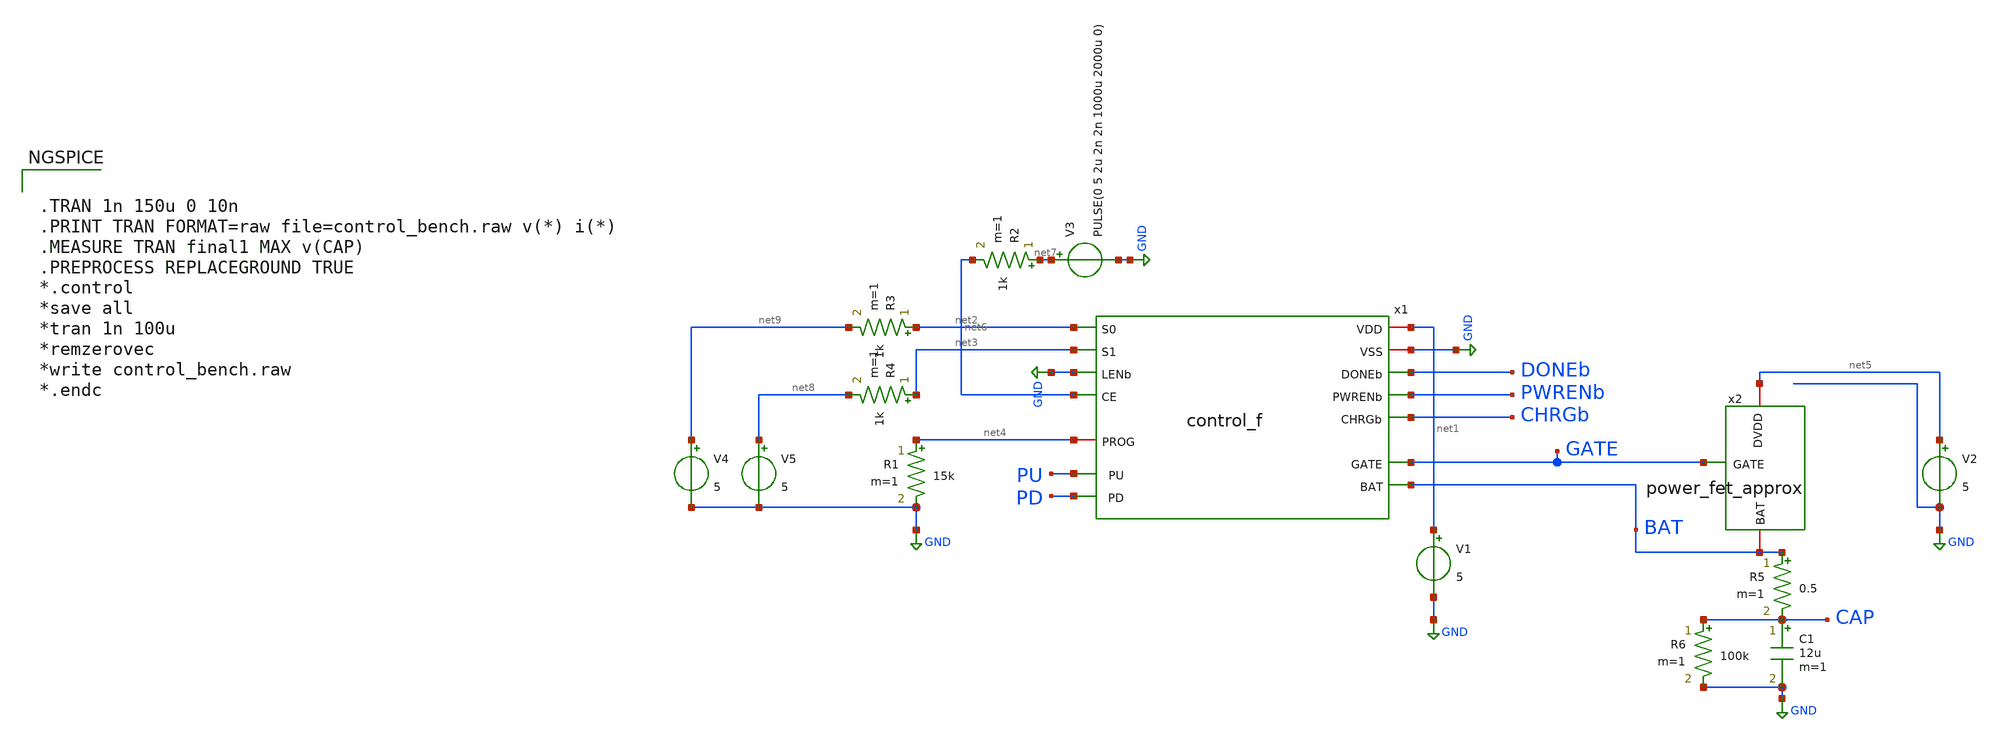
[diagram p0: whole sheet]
** sch_path: analog/xschem/control_bench.sch
**.subckt control_bench
V1 net1 GND 5
R1 net4 GND 15k m=1
R2 net7 net6 1k m=1
V2 net5 GND 5
R3 net2 net9 1k m=1
R4 net3 net8 1k m=1
V3 net7 GND PULSE(0 5 2u 2n 2n 1000u 2000u 0)
C1 CAP GND 12u m=1
R5 BAT CAP 0.5 m=1
R6 CAP GND 100k m=1
x2 net5 GATE BAT power_fet_approx
V4 net9 GND 5
V5 net8 GND 5
x1 net1 GND PD PU PWRENb net4 DONEb CHRGb net2 net3 net6 GND BAT GATE control_f
**** begin user architecture code


.TRAN 1n 150u 0 10n
.PRINT TRAN FORMAT=raw file=control_bench.raw v(*) i(*)
.MEASURE TRAN final1 MAX v(CAP)
.PREPROCESS REPLACEGROUND TRUE
*.control
*save all
*tran 1n 100u
*remzerovec
*write control_bench.raw
*.endc



.include $::PDK_ROOT/gf180mcuD/libs.tech/xyce/design.xyce
.lib $::PDK_ROOT/gf180mcuD/libs.tech/xyce/sm141064.xyce typical
.lib $::PDK_ROOT/gf180mcuD/libs.tech/xyce/sm141064.xyce res_typical
.lib $::PDK_ROOT/gf180mcuD/libs.tech/xyce/sm141064.xyce diode_typical
.lib $::PDK_ROOT/gf180mcuD/libs.tech/xyce/sm141064.xyce mimcap_typical
.lib $::PDK_ROOT/gf180mcuD/libs.tech/xyce/sm141064.xyce cap_mim
.include /run/media/veracrypt1/ws-charge-controller/analog/xschem/extracted/power_fet_f.spice
.include /run/media/veracrypt1/ws-charge-controller/analog/xschem/extracted/control_f.spice

**** end user architecture code
**.ends

* expanding   symbol:  power_fet_approx.sym # of pins=3
** sym_path: analog/xschem/power_fet_approx.sym
** sch_path: analog/xschem/power_fet_approx.sch
.subckt power_fet_approx DVDD GATE BAT
*.iopin DVDD
*.iopin BAT
*.ipin GATE
XM1 BAT GATE DVDD DVDD pfet_06v0 L=1u W=46.72u nf=10 ad='int((nf+1)/2) * W/nf * 0.18u' as='int((nf+2)/2) * W/nf * 0.18u'
+ pd='2*int((nf+1)/2) * (W/nf + 0.18u)' ps='2*int((nf+2)/2) * (W/nf + 0.18u)' nrd='0.18u / W' nrs='0.18u / W'
+ sa=0 sb=0 sd=0 m=7920
XM2 BAT GATE DVDD DVDD pfet_06v0 L=1u W=76.465u nf=10 ad='int((nf+1)/2) * W/nf * 0.18u' as='int((nf+2)/2) * W/nf * 0.18u'
+ pd='2*int((nf+1)/2) * (W/nf + 0.18u)' ps='2*int((nf+2)/2) * (W/nf + 0.18u)' nrd='0.18u / W' nrs='0.18u / W'
+ sa=0 sb=0 sd=0 m=7260
.ends

.GLOBAL GND
.end
